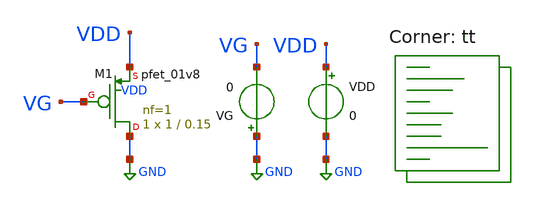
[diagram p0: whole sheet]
** sch_path: week01_mosfet_cmos/tugas1_iv_curve/pfet_iv_curve.sch
**.subckt pfet_iv_curve
XM1 GND VG VDD VDD sky130_fd_pr__pfet_01v8 L=0.15 W=1 nf=1 ad='int((nf+1)/2) * W/nf * 0.29' as='int((nf+2)/2) * W/nf * 0.29'
+ pd='2*int((nf+1)/2) * (W/nf + 0.29)' ps='2*int((nf+2)/2) * (W/nf + 0.29)' nrd='0.29 / W' nrs='0.29 / W'
+ sa=0 sb=0 sd=0 mult=1 m=1
VG GND VG 0
VDD VDD GND 0
**** begin user architecture code
.lib $::SKYWATER_MODELS/sky130.lib.spice tt


.control
	dc VDD 0 1.8 0.1 VG 0 1.8 0.3
	plot i(VDD)
saveall
.endc


**** end user architecture code
**.ends
.GLOBAL GND
.end
